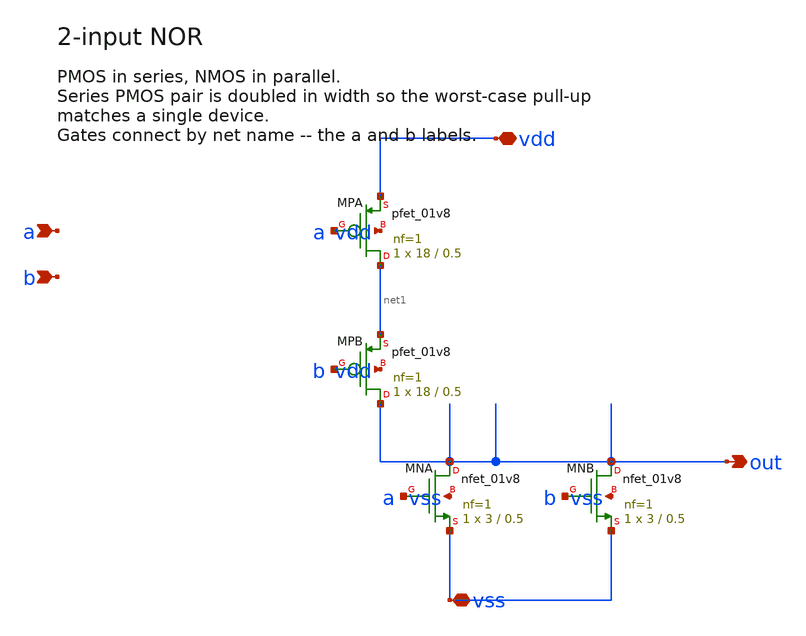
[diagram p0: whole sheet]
** sch_path: common/xschem/nor2.sch
**.subckt nor2 a b out vdd vss
*.ipin a
*.ipin b
*.opin out
*.iopin vdd
*.iopin vss
XMPA net1 a vdd vdd sky130_fd_pr__pfet_01v8 L=0.5 W=18 nf=1 ad='int((nf+1)/2) * W/nf * 0.29' as='int((nf+2)/2) * W/nf * 0.29'
+ pd='2*int((nf+1)/2) * (W/nf + 0.29)' ps='2*int((nf+2)/2) * (W/nf + 0.29)' nrd='0.29 / W' nrs='0.29 / W'
+ sa=0 sb=0 sd=0 mult=1 m=1
XMPB out b net1 vdd sky130_fd_pr__pfet_01v8 L=0.5 W=18 nf=1 ad='int((nf+1)/2) * W/nf * 0.29' as='int((nf+2)/2) * W/nf * 0.29'
+ pd='2*int((nf+1)/2) * (W/nf + 0.29)' ps='2*int((nf+2)/2) * (W/nf + 0.29)' nrd='0.29 / W' nrs='0.29 / W'
+ sa=0 sb=0 sd=0 mult=1 m=1
XMNA out a vss vss sky130_fd_pr__nfet_01v8 L=0.5 W=3 nf=1 ad='int((1 + 1)/2) * 3 / 1 * 0.29' as='int((1 + 2)/2) * 3 / 1 * 0.29'
+ pd='2*int((1 + 1)/2) * (3 / 1 + 0.29)' ps='2*int((1 + 2)/2) * (3 / 1 + 0.29)' nrd='0.29 / 3 ' nrs='0.29 / 3 '
+ sa=0 sb=0 sd=0 mult=1 m=1
XMNB out b vss vss sky130_fd_pr__nfet_01v8 L=0.5 W=3 nf=1 ad='int((1 + 1)/2) * 3 / 1 * 0.29' as='int((1 + 2)/2) * 3 / 1 * 0.29'
+ pd='2*int((1 + 1)/2) * (3 / 1 + 0.29)' ps='2*int((1 + 2)/2) * (3 / 1 + 0.29)' nrd='0.29 / 3 ' nrs='0.29 / 3 '
+ sa=0 sb=0 sd=0 mult=1 m=1
**.ends
.end
